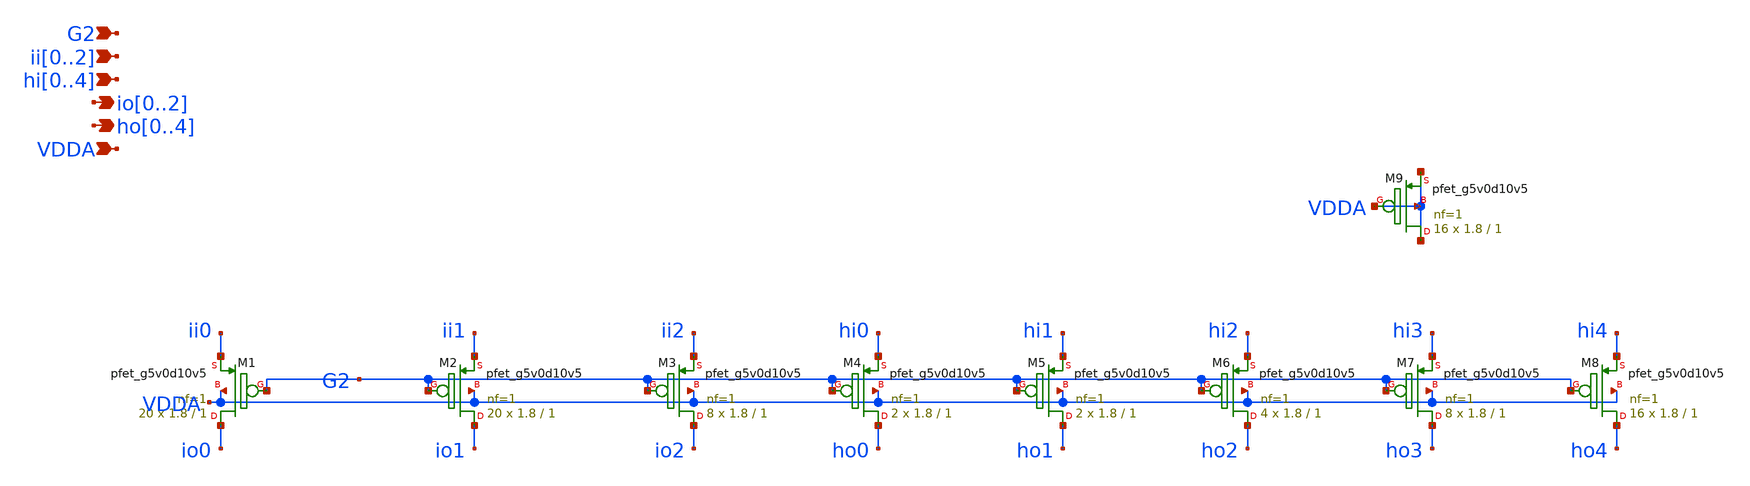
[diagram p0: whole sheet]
** sch_path: xschem/cm_pcell2.sch
**.subckt cm_pcell2 G2 io0,io1,io2 VDDA ho0,ho1,ho2,ho3,ho4 ii0,ii1,ii2 hi0,hi1,hi2,hi3,hi4
*.ipin G2
*.opin io0,io1,io2
*.ipin VDDA
*.opin ho0,ho1,ho2,ho3,ho4
*.ipin ii0,ii1,ii2
*.ipin hi0,hi1,hi2,hi3,hi4
XM1 io0 G2 ii0 VDDA sky130_fd_pr__pfet_g5v0d10v5 L=1 W=1.8 nf=1 ad='int((nf+1)/2) * W/nf * 0.29' as='int((nf+2)/2) * W/nf * 0.29'
+ pd='2*int((nf+1)/2) * (W/nf + 0.29)' ps='2*int((nf+2)/2) * (W/nf + 0.29)' nrd='0.29 / W' nrs='0.29 / W'
+ sa=0 sb=0 sd=0 mult=20 m=20
XM2 io1 G2 ii1 VDDA sky130_fd_pr__pfet_g5v0d10v5 L=1 W=1.8 nf=1 ad='int((nf+1)/2) * W/nf * 0.29' as='int((nf+2)/2) * W/nf * 0.29'
+ pd='2*int((nf+1)/2) * (W/nf + 0.29)' ps='2*int((nf+2)/2) * (W/nf + 0.29)' nrd='0.29 / W' nrs='0.29 / W'
+ sa=0 sb=0 sd=0 mult=20 m=20
XM3 io2 G2 ii2 VDDA sky130_fd_pr__pfet_g5v0d10v5 L=1 W=1.8 nf=1 ad='int((nf+1)/2) * W/nf * 0.29' as='int((nf+2)/2) * W/nf * 0.29'
+ pd='2*int((nf+1)/2) * (W/nf + 0.29)' ps='2*int((nf+2)/2) * (W/nf + 0.29)' nrd='0.29 / W' nrs='0.29 / W'
+ sa=0 sb=0 sd=0 mult=8 m=8
XM4 ho0 G2 hi0 VDDA sky130_fd_pr__pfet_g5v0d10v5 L=1 W=1.8 nf=1 ad='int((nf+1)/2) * W/nf * 0.29' as='int((nf+2)/2) * W/nf * 0.29'
+ pd='2*int((nf+1)/2) * (W/nf + 0.29)' ps='2*int((nf+2)/2) * (W/nf + 0.29)' nrd='0.29 / W' nrs='0.29 / W'
+ sa=0 sb=0 sd=0 mult=2 m=2
XM6 ho2 G2 hi2 VDDA sky130_fd_pr__pfet_g5v0d10v5 L=1 W=1.8 nf=1 ad='int((nf+1)/2) * W/nf * 0.29' as='int((nf+2)/2) * W/nf * 0.29'
+ pd='2*int((nf+1)/2) * (W/nf + 0.29)' ps='2*int((nf+2)/2) * (W/nf + 0.29)' nrd='0.29 / W' nrs='0.29 / W'
+ sa=0 sb=0 sd=0 mult=4 m=4
XM7 ho3 G2 hi3 VDDA sky130_fd_pr__pfet_g5v0d10v5 L=1 W=1.8 nf=1 ad='int((nf+1)/2) * W/nf * 0.29' as='int((nf+2)/2) * W/nf * 0.29'
+ pd='2*int((nf+1)/2) * (W/nf + 0.29)' ps='2*int((nf+2)/2) * (W/nf + 0.29)' nrd='0.29 / W' nrs='0.29 / W'
+ sa=0 sb=0 sd=0 mult=8 m=8
XM8 ho4 G2 hi4 VDDA sky130_fd_pr__pfet_g5v0d10v5 L=1 W=1.8 nf=1 ad='int((nf+1)/2) * W/nf * 0.29' as='int((nf+2)/2) * W/nf * 0.29'
+ pd='2*int((nf+1)/2) * (W/nf + 0.29)' ps='2*int((nf+2)/2) * (W/nf + 0.29)' nrd='0.29 / W' nrs='0.29 / W'
+ sa=0 sb=0 sd=0 mult=16 m=16
XM5 ho1 G2 hi1 VDDA sky130_fd_pr__pfet_g5v0d10v5 L=1 W=1.8 nf=1 ad='int((nf+1)/2) * W/nf * 0.29' as='int((nf+2)/2) * W/nf * 0.29'
+ pd='2*int((nf+1)/2) * (W/nf + 0.29)' ps='2*int((nf+2)/2) * (W/nf + 0.29)' nrd='0.29 / W' nrs='0.29 / W'
+ sa=0 sb=0 sd=0 mult=2 m=2
XM9 VDDA VDDA VDDA VDDA sky130_fd_pr__pfet_g5v0d10v5 L=1 W=1.8 nf=1 ad='int((nf+1)/2) * W/nf * 0.29'
+ as='int((nf+2)/2) * W/nf * 0.29' pd='2*int((nf+1)/2) * (W/nf + 0.29)' ps='2*int((nf+2)/2) * (W/nf + 0.29)'
+ nrd='0.29 / W' nrs='0.29 / W' sa=0 sb=0 sd=0 mult=16 m=16
**.ends
.end
